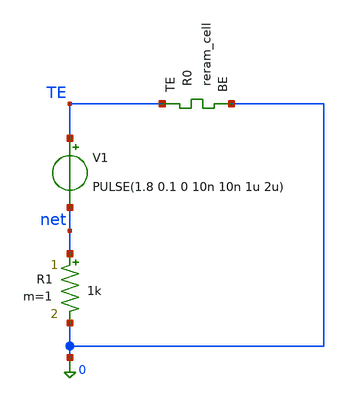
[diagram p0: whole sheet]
** sch_path: memristor_models/sky130_original/1R.sch
**.subckt 1R
V1 TE net PULSE(1.8 0.1 0 10n 10n 1u 2u)
XR0 TE 0 sky130_fd_pr_reram__reram_cell Tfilament_0=3.3e-9
R1 net 0 1k m=1
**** begin user architecture code

** opencircuitdesign pdks install
.inc $::SKYWATER_MODELS/sky130_fd_pr_reram__reram_cell.spice



.option savecurrents
.tran 100n 1000u
.control
	save all
	run
	write 1R.raw
.endc



**** end user architecture code
**.ends
.end
